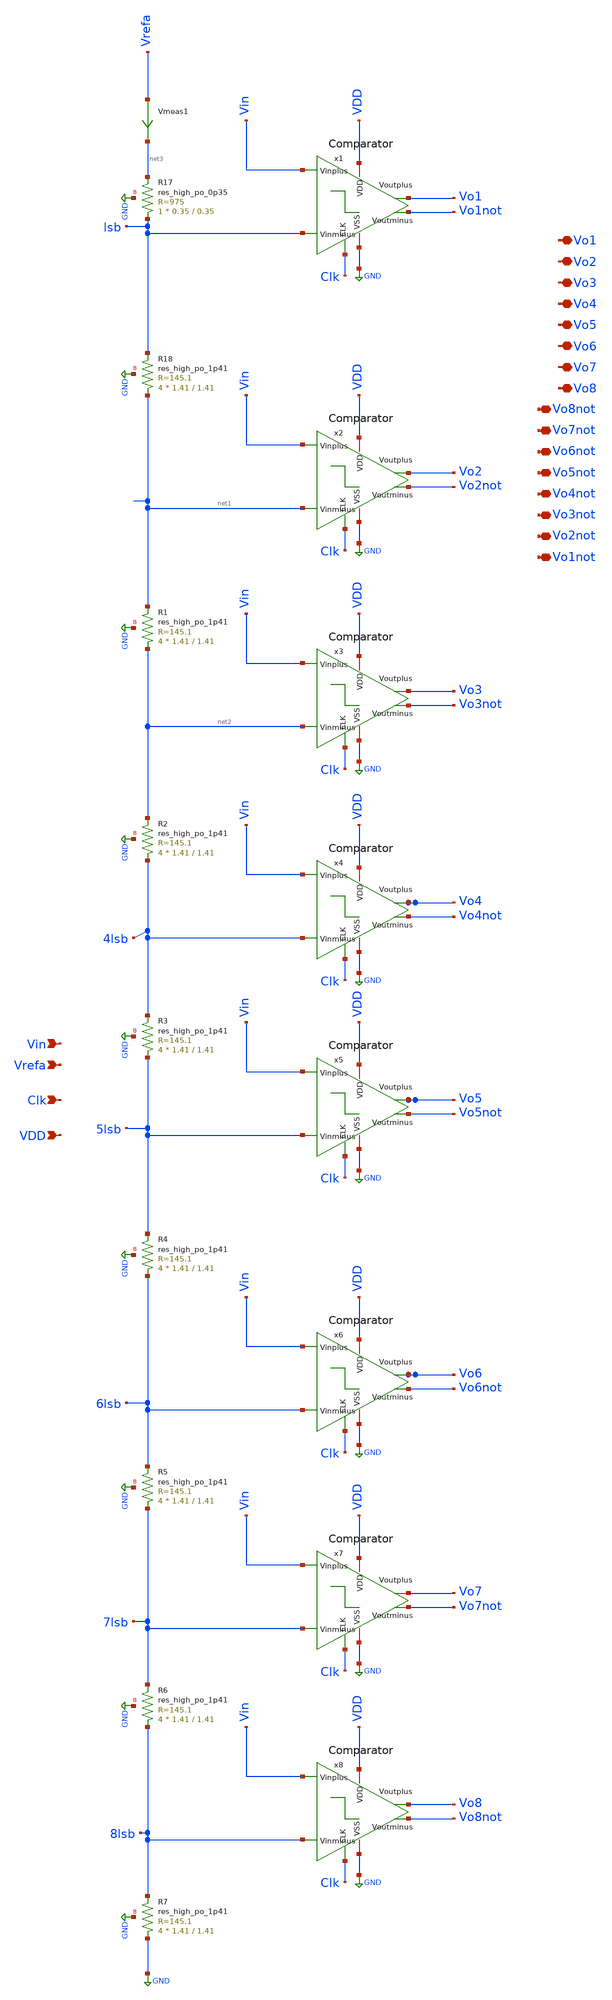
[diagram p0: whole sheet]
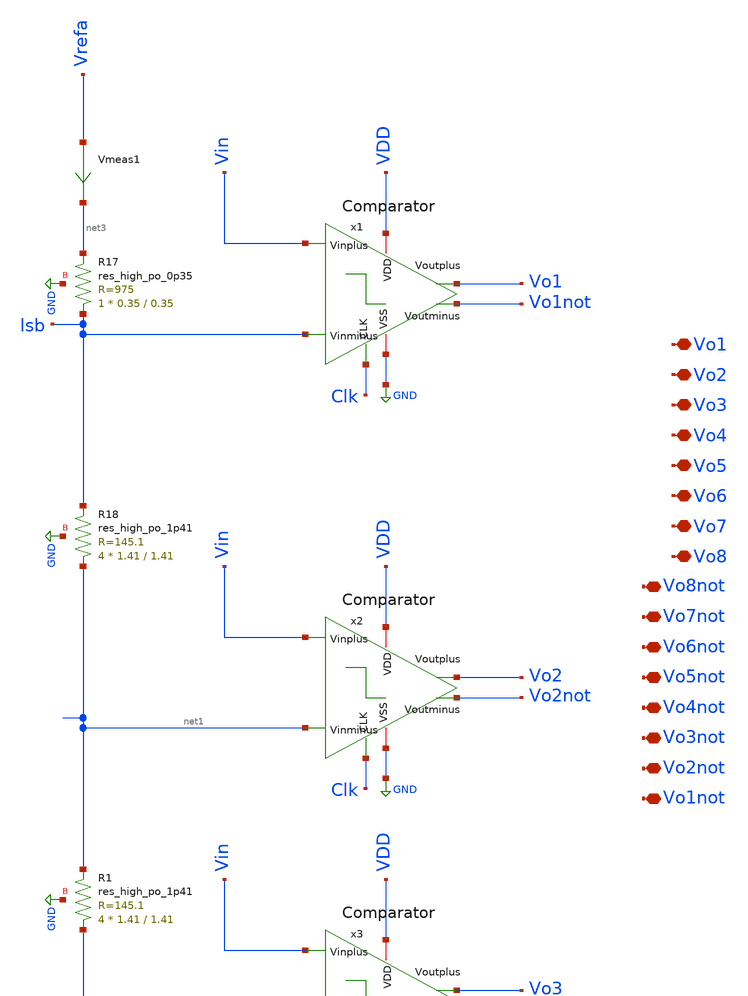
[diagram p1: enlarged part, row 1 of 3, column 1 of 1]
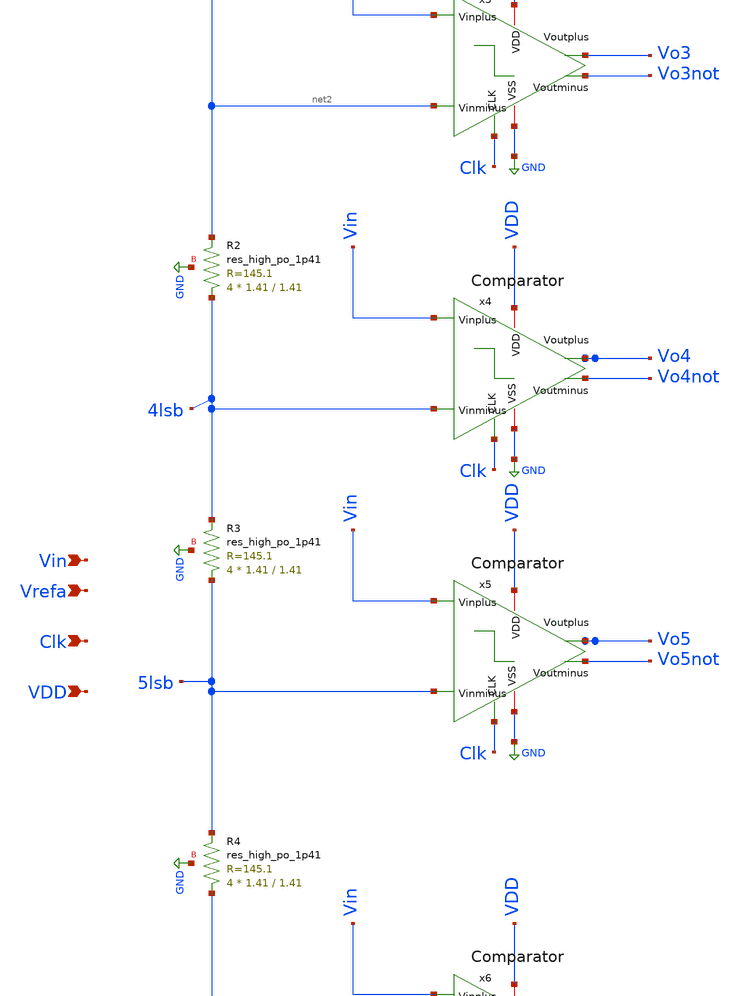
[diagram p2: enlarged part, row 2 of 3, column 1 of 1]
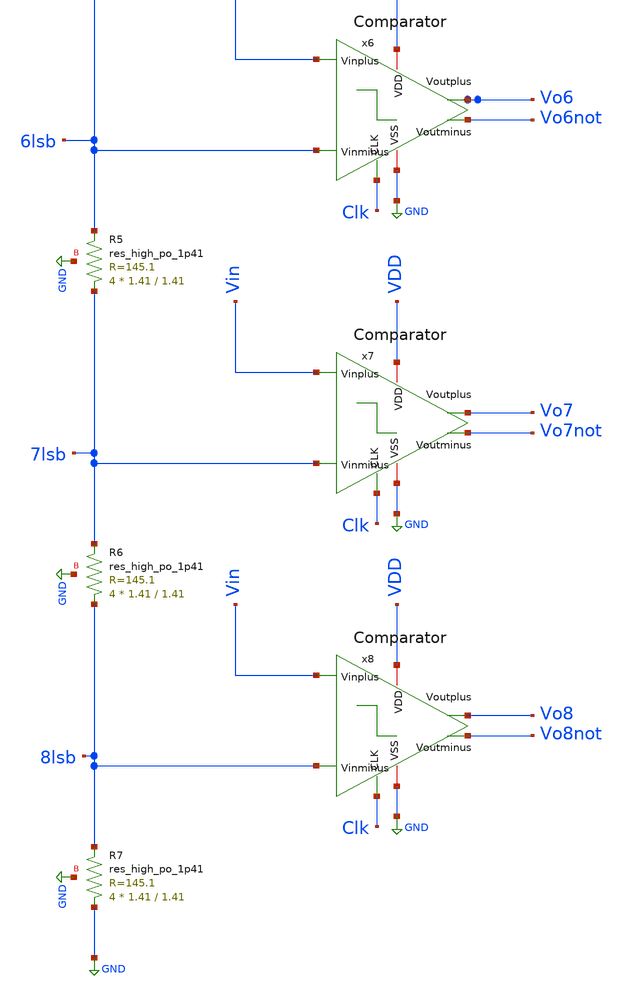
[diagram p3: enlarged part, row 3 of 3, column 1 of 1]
** sch_path: DataConverters/3bitADC.sch
**.subckt 3bitADC Vin Vrefa Clk VDD Vo1 Vo2 Vo3 Vo4 Vo5 Vo6 Vo7 Vo8 Vo8not Vo7not Vo6not Vo5not
*+ Vo4not Vo3not Vo2not Vo1not
*.ipin Vin
*.ipin Vrefa
*.ipin Clk
*.ipin VDD
*.iopin Vo1
*.iopin Vo2
*.iopin Vo3
*.iopin Vo4
*.iopin Vo5
*.iopin Vo6
*.iopin Vo7
*.iopin Vo8
*.iopin Vo8not
*.iopin Vo7not
*.iopin Vo6not
*.iopin Vo5not
*.iopin Vo4not
*.iopin Vo3not
*.iopin Vo2not
*.iopin Vo1not
Vmeas1 Vrefa net3 0
.save i(vmeas1)
x1 VDD Vo1not Vo1 Clk Vin lsb GND Comparator
x2 VDD Vo2not Vo2 Clk Vin net1 GND Comparator
x3 VDD Vo3not Vo3 Clk Vin net2 GND Comparator
x4 VDD Vo4not Vo4 Clk Vin 4lsb GND Comparator
x5 VDD Vo5not Vo5 Clk Vin 5lsb GND Comparator
x6 VDD Vo6not Vo6 Clk Vin 6lsb GND Comparator
x7 VDD Vo7not Vo7 Clk Vin 7lsb GND Comparator
x8 VDD Vo8not Vo8 Clk Vin 8lsb GND Comparator
XR18 net1 lsb GND sky130_fd_pr__res_high_po_1p41 L=1.41 mult=4 m=4
XR1 net2 net1 GND sky130_fd_pr__res_high_po_1p41 L=1.41 mult=4 m=4
XR2 4lsb net2 GND sky130_fd_pr__res_high_po_1p41 L=1.41 mult=4 m=4
XR3 5lsb 4lsb GND sky130_fd_pr__res_high_po_1p41 L=1.41 mult=4 m=4
XR4 6lsb 5lsb GND sky130_fd_pr__res_high_po_1p41 L=1.41 mult=4 m=4
XR5 7lsb 6lsb GND sky130_fd_pr__res_high_po_1p41 L=1.41 mult=4 m=4
XR6 8lsb 7lsb GND sky130_fd_pr__res_high_po_1p41 L=1.41 mult=4 m=4
XR7 GND 8lsb GND sky130_fd_pr__res_high_po_1p41 L=1.41 mult=4 m=4
XR17 lsb net3 GND sky130_fd_pr__res_high_po_0p35 L=0.35 mult=1 m=1
**.ends
.GLOBAL GND
.end
